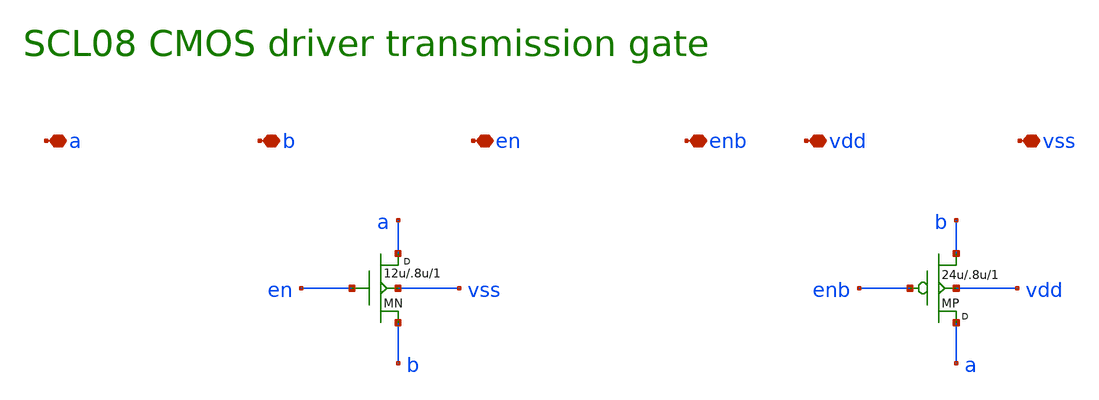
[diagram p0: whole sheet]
** sch_path: ICMC/schematic/icm_drive_tg08.sch
**.subckt icm_drive_tg08 a b en enb vdd vss
*.iopin a
*.iopin b
*.iopin en
*.iopin enb
*.iopin vdd
*.iopin vss
MN a en b vss N w=12u l=.8u ad=54p as=54p pd=33u ps=33u m=1
MP a enb b vdd P w=24u l=.8u ad=108p as=108p pd=57u ps=57u m=1
**.ends
.end
